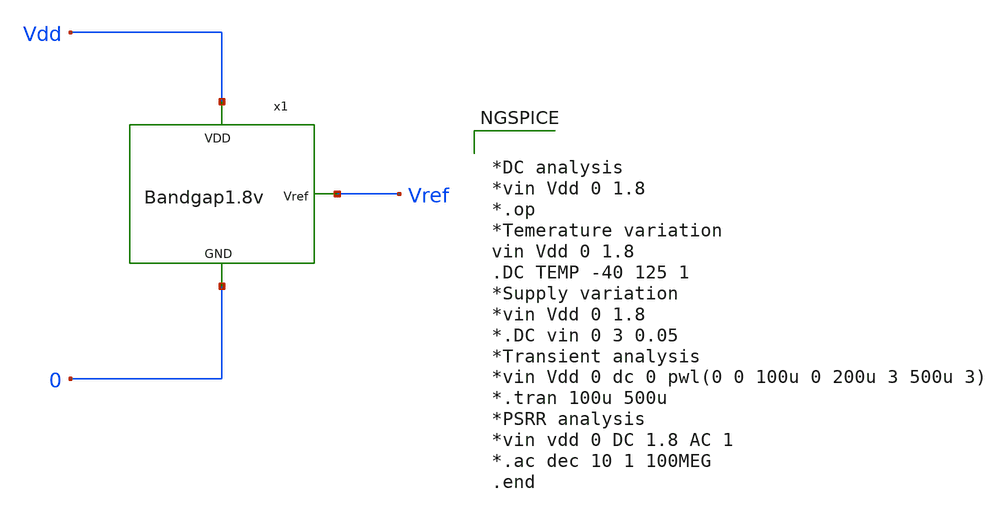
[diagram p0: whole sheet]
** sch_path: Bandgap/Schematics/BGR1.8v/Bandgap1.8v_TB.sch
**.subckt Bandgap1.8v_TB
x1 Vref Vdd 0 Bandgap1.8v
**** begin user architecture code


*DC analysis
*vin Vdd 0 1.8
*.op
*Temerature variation
vin Vdd 0 1.8
.DC TEMP -40 125 1
*Supply variation
*vin Vdd 0 1.8
*.DC vin 0 3 0.05
*Transient analysis
*vin Vdd 0 dc 0 pwl(0 0 100u 0 200u 3 500u 3)
*.tran 100u 500u
*PSRR analysis
*vin vdd 0 DC 1.8 AC 1
*.ac dec 10 1 100MEG
.end



.include $::SKYWATER_MODELS/cells/nfet_01v8/sky130_fd_pr__nfet_01v8__tt.corner.spice
.include $::SKYWATER_MODELS/cells/nfet_01v8_lvt/sky130_fd_pr__nfet_01v8_lvt__tt.corner.spice
.include $::SKYWATER_MODELS/cells/pfet_01v8/sky130_fd_pr__pfet_01v8__tt.corner.spice
.include $::SKYWATER_MODELS/cells/nfet_03v3_nvt/sky130_fd_pr__nfet_03v3_nvt__tt.corner.spice
.include $::SKYWATER_MODELS/cells/nfet_05v0_nvt/sky130_fd_pr__nfet_05v0_nvt__tt.corner.spice
.include $::SKYWATER_MODELS/cells/esd_nfet_01v8/sky130_fd_pr__esd_nfet_01v8__tt.corner.spice
.include $::SKYWATER_MODELS/cells/pfet_01v8_lvt/sky130_fd_pr__pfet_01v8_lvt__tt.corner.spice
.include $::SKYWATER_MODELS/cells/pfet_01v8_hvt/sky130_fd_pr__pfet_01v8_hvt__tt.corner.spice
.include $::SKYWATER_MODELS/cells/esd_pfet_g5v0d10v5/sky130_fd_pr__esd_pfet_g5v0d10v5__tt.corner.spice
.include $::SKYWATER_MODELS/cells/pfet_g5v0d10v5/sky130_fd_pr__pfet_g5v0d10v5__tt.corner.spice
.include $::SKYWATER_MODELS/cells/pfet_g5v0d16v0/sky130_fd_pr__pfet_g5v0d16v0__tt.corner.spice
.include $::SKYWATER_MODELS/cells/nfet_g5v0d10v5/sky130_fd_pr__nfet_g5v0d10v5__tt.corner.spice
.include $::SKYWATER_MODELS/cells/nfet_g5v0d16v0/sky130_fd_pr__nfet_g5v0d16v0__tt_discrete.corner.spice
.include $::SKYWATER_MODELS/cells/esd_nfet_g5v0d10v5/sky130_fd_pr__esd_nfet_g5v0d10v5__tt.corner.spice
.include $::SKYWATER_MODELS/models/corners/tt/nonfet.spice
* Mismatch parameters
.include $::SKYWATER_MODELS/cells/nfet_01v8/sky130_fd_pr__nfet_01v8__mismatch.corner.spice
.include $::SKYWATER_MODELS/cells/pfet_01v8/sky130_fd_pr__pfet_01v8__mismatch.corner.spice
.include $::SKYWATER_MODELS/cells/nfet_01v8_lvt/sky130_fd_pr__nfet_01v8_lvt__mismatch.corner.spice
.include $::SKYWATER_MODELS/cells/pfet_01v8_lvt/sky130_fd_pr__pfet_01v8_lvt__mismatch.corner.spice
.include $::SKYWATER_MODELS/cells/pfet_01v8_hvt/sky130_fd_pr__pfet_01v8_hvt__mismatch.corner.spice
.include $::SKYWATER_MODELS/cells/nfet_g5v0d10v5/sky130_fd_pr__nfet_g5v0d10v5__mismatch.corner.spice
.include $::SKYWATER_MODELS/cells/pfet_g5v0d10v5/sky130_fd_pr__pfet_g5v0d10v5__mismatch.corner.spice
.include $::SKYWATER_MODELS/cells/nfet_05v0_nvt/sky130_fd_pr__nfet_05v0_nvt__mismatch.corner.spice
.include $::SKYWATER_MODELS/cells/nfet_03v3_nvt/sky130_fd_pr__nfet_03v3_nvt__mismatch.corner.spice
* Resistor$::SKYWATER_MODELS/Capacitor
.include $::SKYWATER_MODELS/models/r+c/res_typical__cap_typical.spice
.include $::SKYWATER_MODELS/models/r+c/res_typical__cap_typical__lin.spice
* Special cells
.include $::SKYWATER_MODELS/models/corners/tt/specialized_cells.spice
* All models
.include $::SKYWATER_MODELS/models/all.spice
* Corner
.include $::SKYWATER_MODELS/models/corners/tt/rf.spice

**** end user architecture code
**.ends
.end
